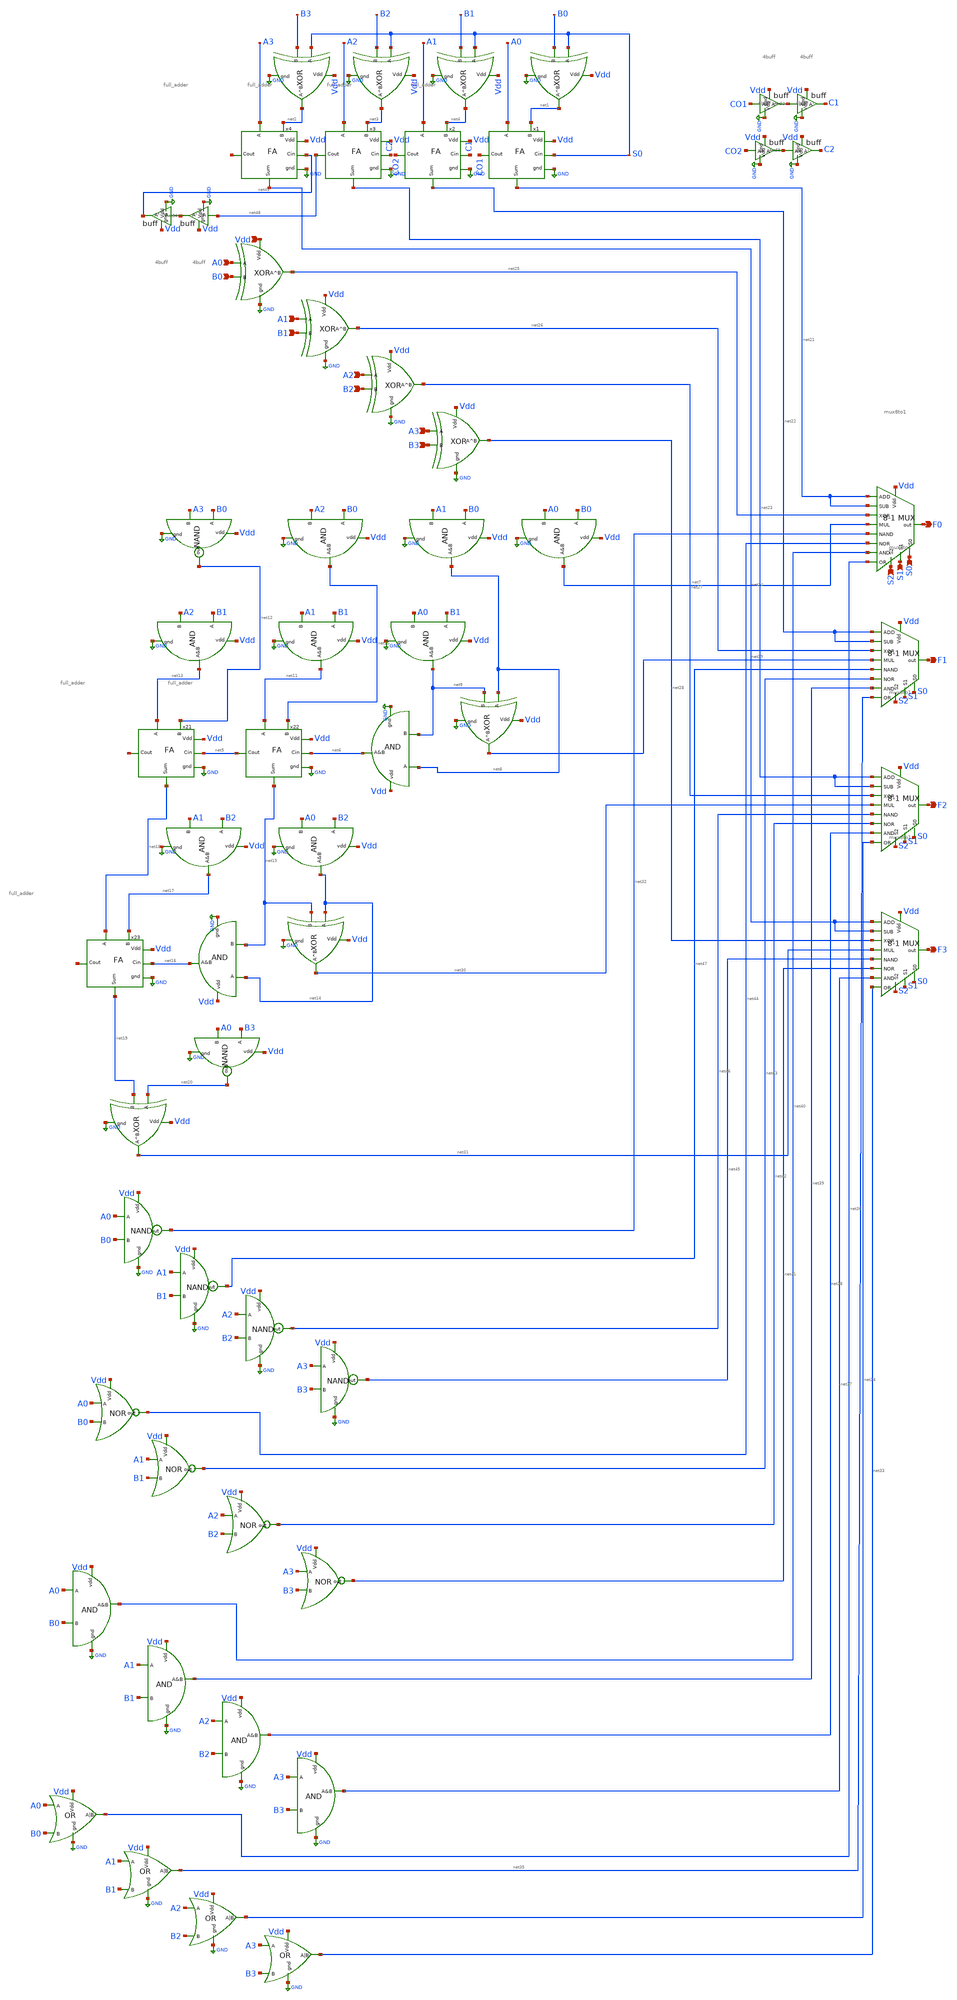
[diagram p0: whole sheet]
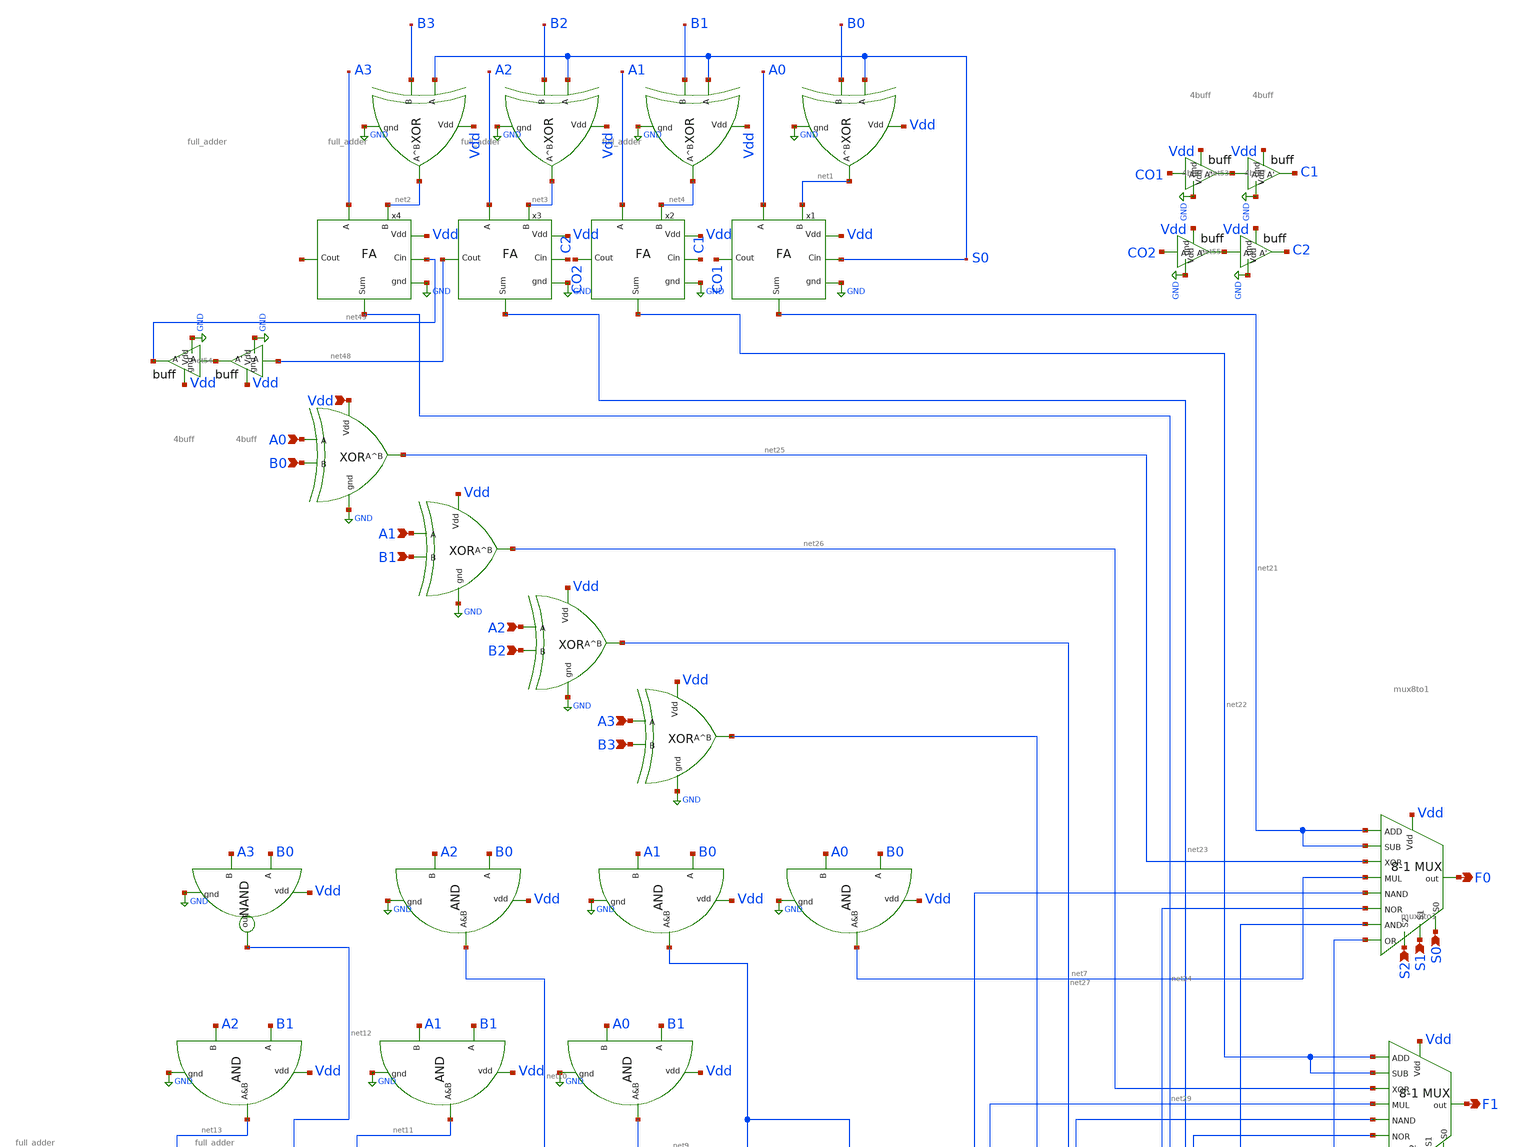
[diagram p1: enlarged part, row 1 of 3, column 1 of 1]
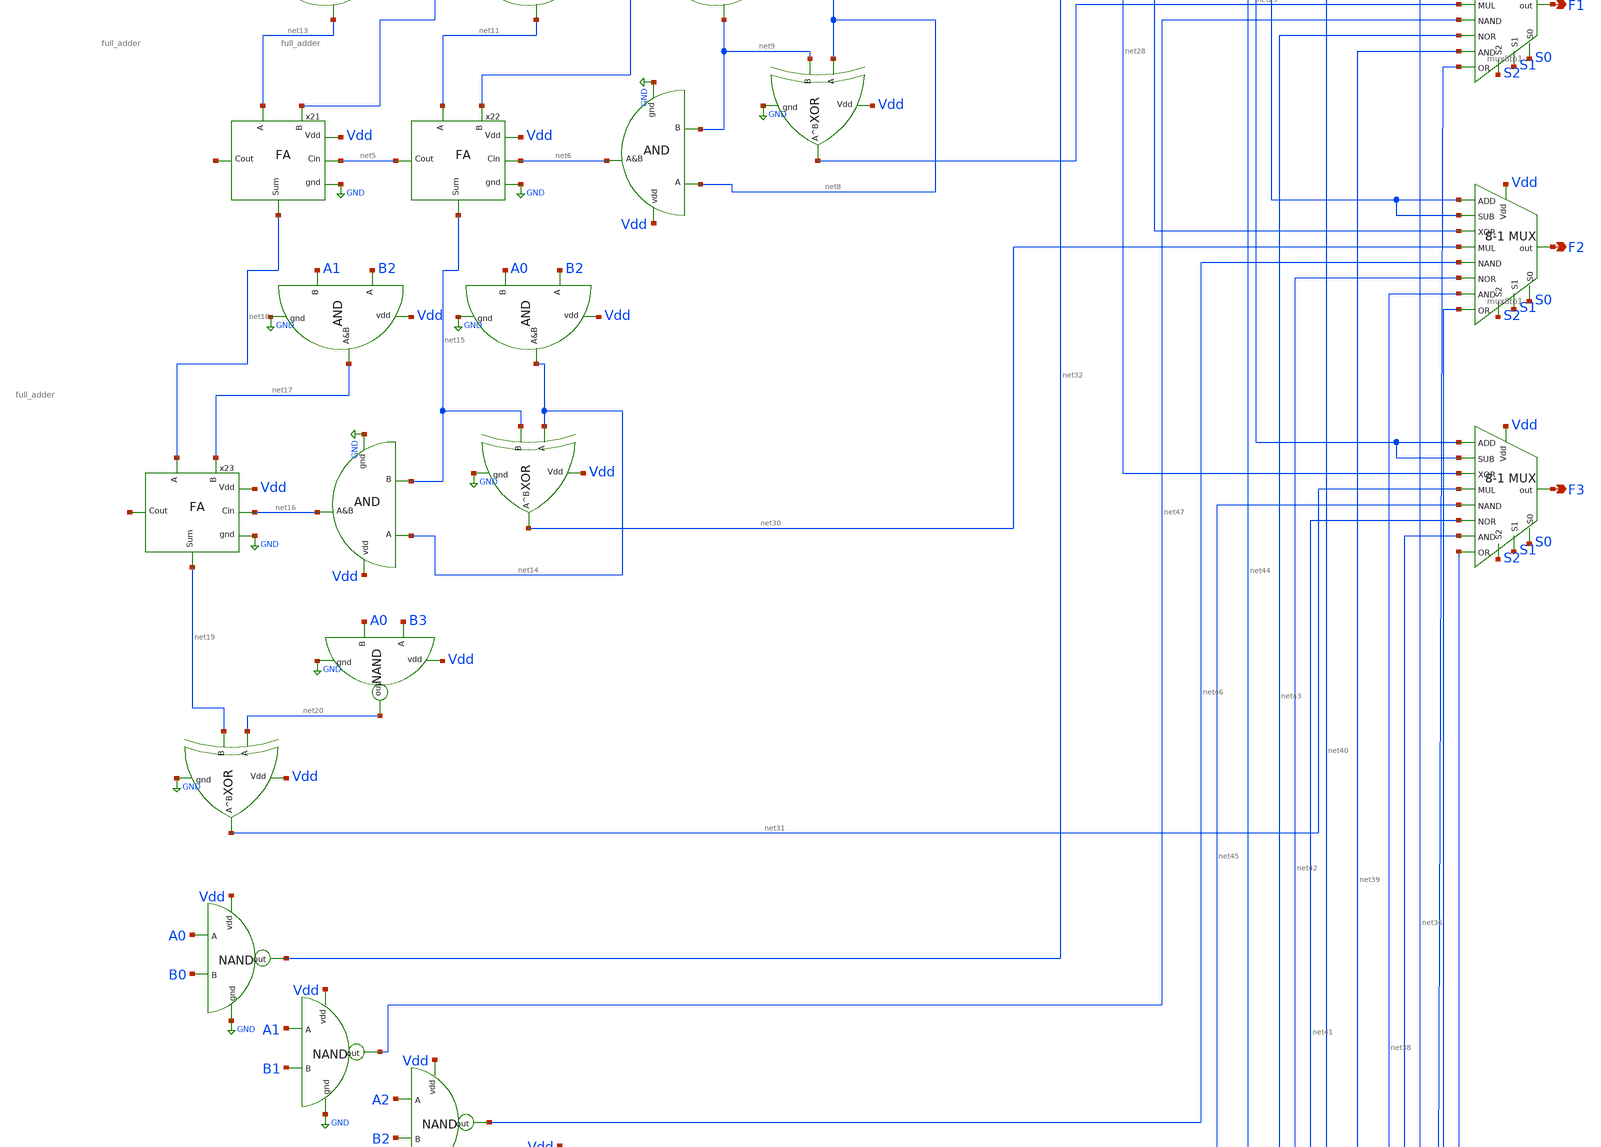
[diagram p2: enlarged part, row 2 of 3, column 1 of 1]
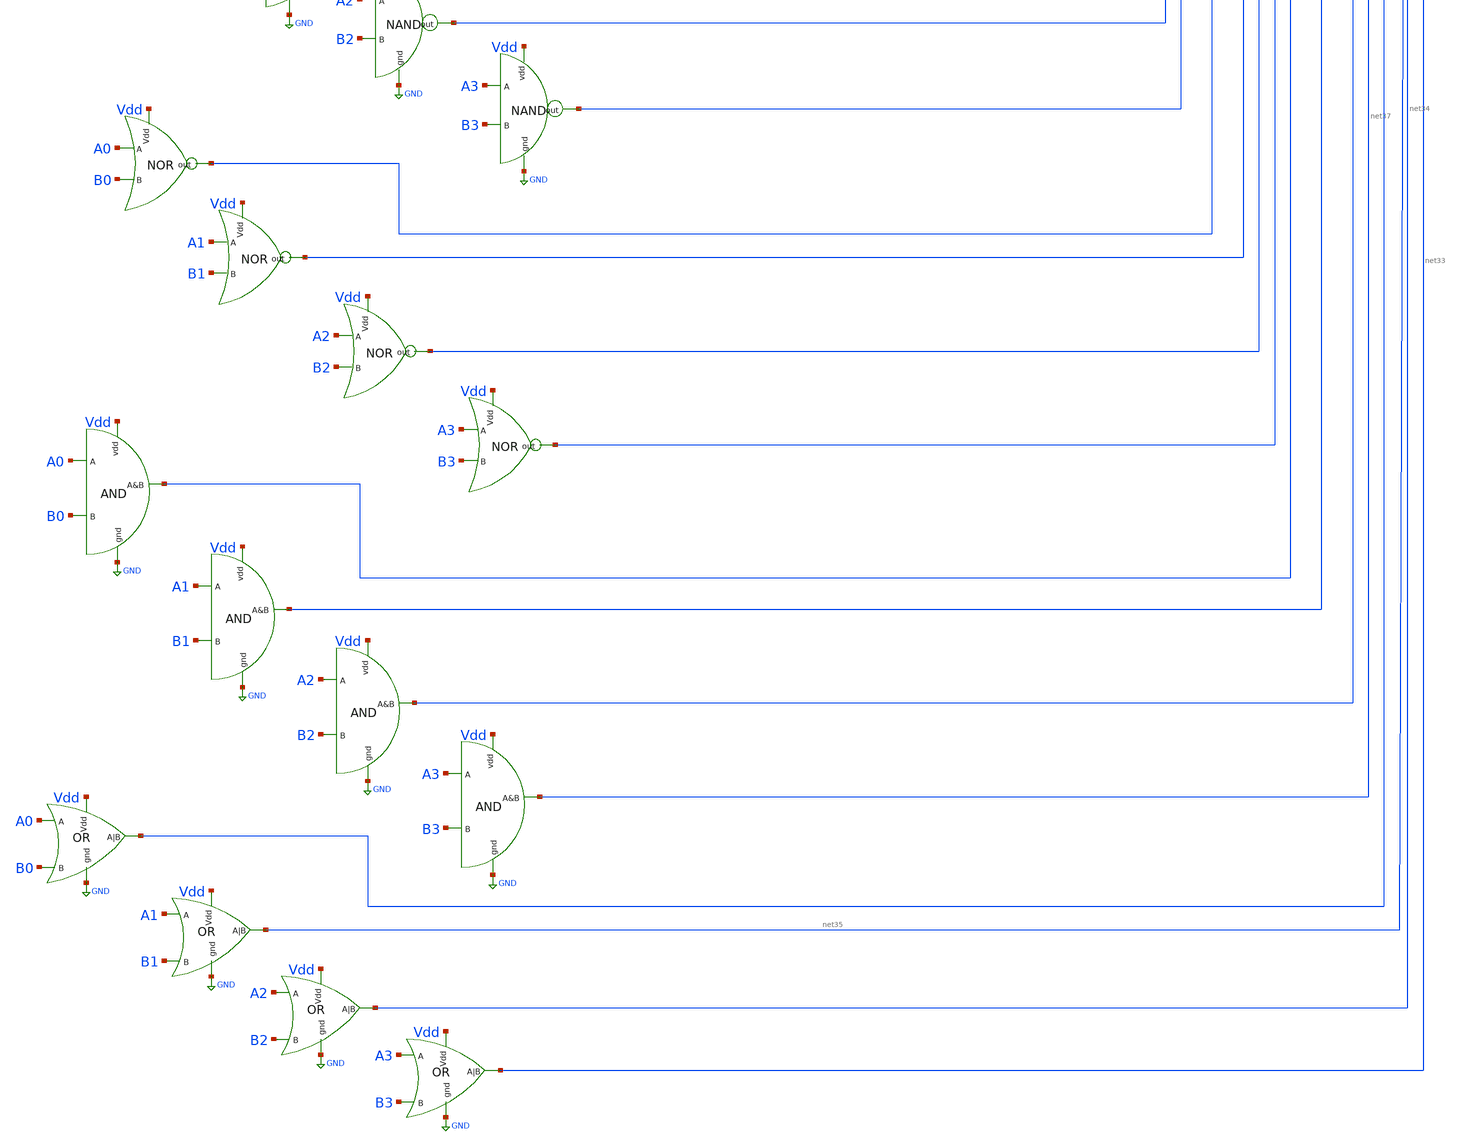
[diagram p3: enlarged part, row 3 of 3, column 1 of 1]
** sch_path: extra_stuff/alu.sch
**.subckt alu A0 B0 A1 B1 A2 B2 A3 B3 Vdd S2 S1 S0 F0 F1 F2 F3
*.ipin A0
*.ipin B0
*.ipin A1
*.ipin B1
*.ipin A2
*.ipin B2
*.ipin A3
*.ipin B3
*.ipin Vdd
*.ipin S2
*.ipin S1
*.ipin S0
*.opin F0
*.opin F1
*.opin F2
*.opin F3
x1 net21 CO1 S0 Vdd GND A0 net1 full_adder
x2 net22 CO2 C1 Vdd GND A1 net4 full_adder
x3 net23 net48 C2 Vdd GND A2 net3 full_adder
x4 net24 net50 net49 Vdd GND A3 net2 full_adder
x5 Vdd GND net1 S0 B0 xor
x6 Vdd GND net4 S0 B1 xor
x7 Vdd GND net3 S0 B2 xor
x8 Vdd GND net2 S0 B3 xor
x9 Vdd GND net25 A0 B0 xor
x10 A0 B0 net40 Vdd GND and
x11 Vdd GND net36 A0 B0 or
x12 Vdd GND net26 A1 B1 xor
x13 Vdd GND net27 A2 B2 xor
x14 A1 B1 net39 Vdd GND and
x15 A2 B2 net38 Vdd GND and
x16 Vdd GND net28 A3 B3 xor
x17 A3 B3 net37 Vdd GND and
x18 Vdd GND net35 A1 B1 or
x19 Vdd GND net34 A2 B2 or
x20 Vdd GND net33 A3 B3 or
x21 net18 net51 net5 Vdd GND net13 net12 full_adder
x22 net15 net5 net6 Vdd GND net11 net10 full_adder
x23 net19 net52 net16 Vdd GND net18 net17 full_adder
x24 Vdd GND net29 net8 net9 xor
x25 net8 net9 net6 Vdd GND and
x26 net12 Vdd B0 A3 GND NAND
x27 B0 A2 net10 Vdd GND and
x28 B0 A1 net8 Vdd GND and
x29 B0 A0 net7 Vdd GND and
x30 B1 A2 net13 Vdd GND and
x31 B1 A1 net11 Vdd GND and
x32 B1 A0 net9 Vdd GND and
x33 B2 A1 net17 Vdd GND and
x34 B2 A0 net14 Vdd GND and
x35 Vdd GND net30 net14 net15 xor
x36 net14 net15 net16 Vdd GND and
x37 Vdd GND net31 net20 net19 xor
x38 net20 Vdd B3 A0 GND NAND
x39 net32 Vdd A0 B0 GND NAND
x40 net47 Vdd A1 B1 GND NAND
x41 net46 Vdd A2 B2 GND NAND
x42 net45 Vdd A3 B3 GND NAND
x43 net44 Vdd A0 B0 nor
x44 net43 Vdd A1 B1 nor
x45 net42 Vdd A2 B2 nor
x46 net41 Vdd A3 B3 nor
x47 F0 net21 net21 net25 net7 Vdd net32 net44 net40 net36 S0 S1 S2 mux8to1
x48 F1 net22 net22 net26 net29 Vdd net47 net43 net39 net35 S0 S1 S2 mux8to1
x49 F2 net23 net23 net27 net30 Vdd net46 net42 net38 net34 S0 S1 S2 mux8to1
x50 F3 net24 net24 net28 net31 Vdd net45 net41 net37 net33 S0 S1 S2 mux8to1
x51 net53 GND CO1 Vdd 4buff
x54 C1 GND net53 Vdd 4buff
x57 net54 GND net48 Vdd 4buff
x58 net49 GND net54 Vdd 4buff
x52 net55 GND CO2 Vdd 4buff
x55 C2 GND net55 Vdd 4buff
**.ends
.GLOBAL GND
.end
